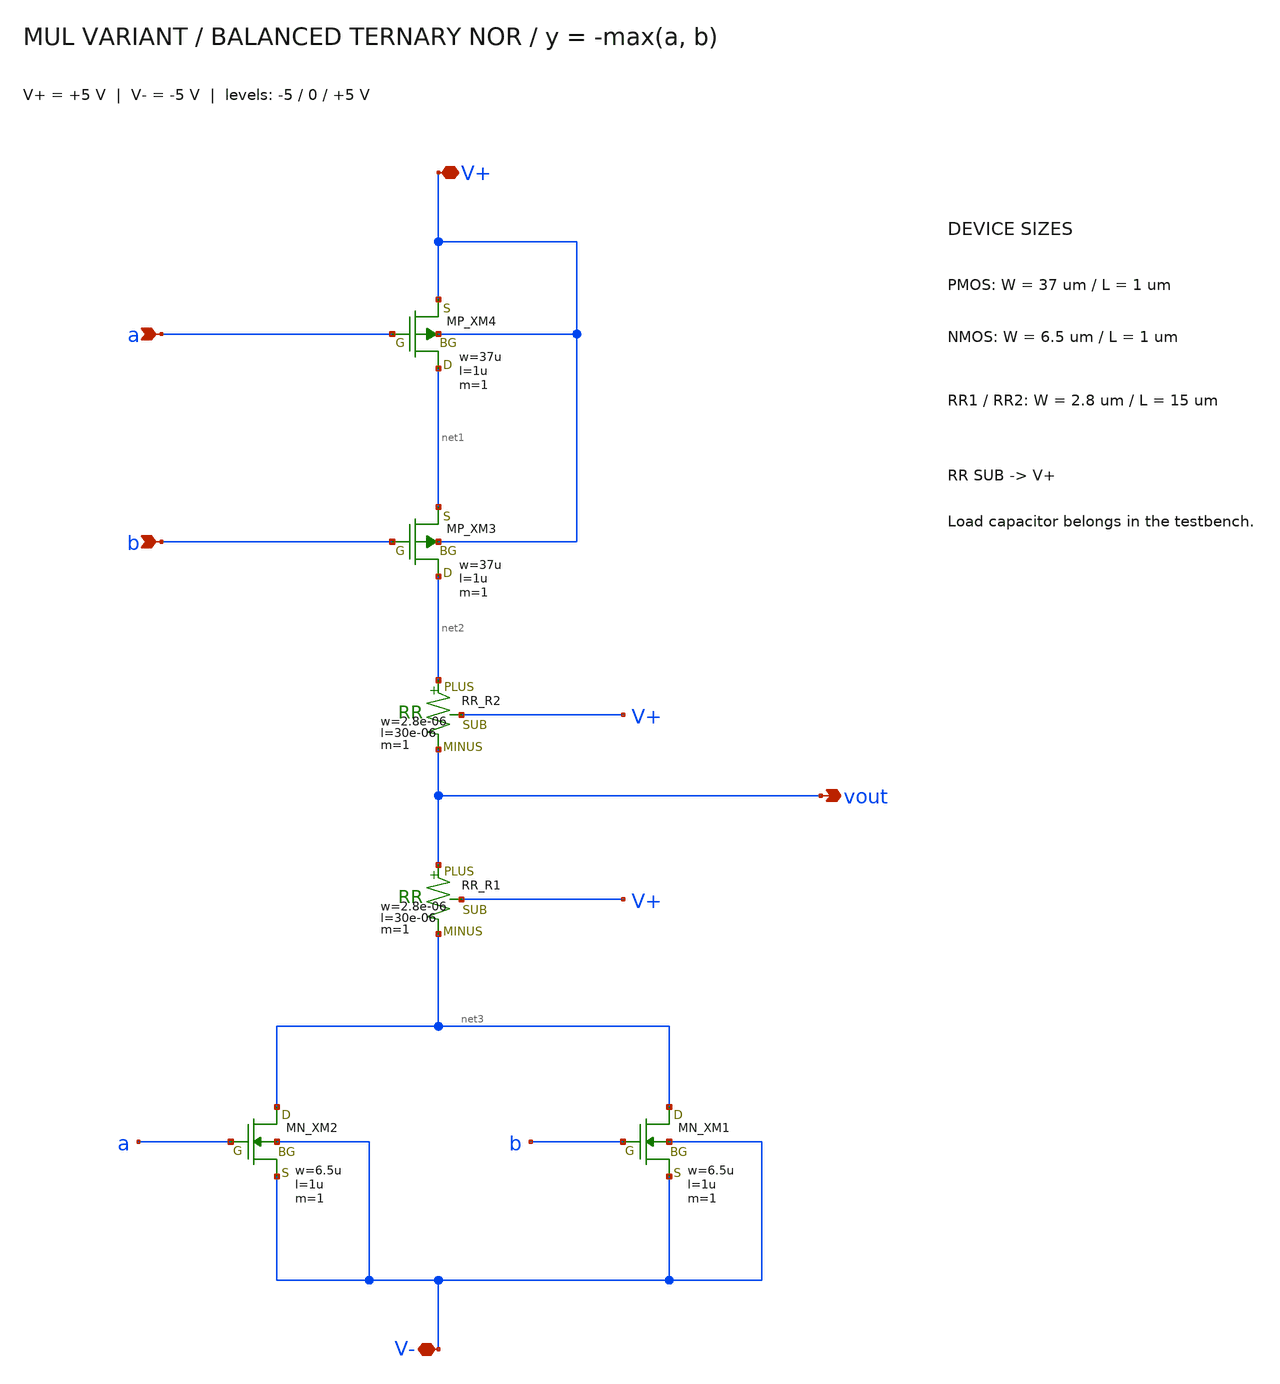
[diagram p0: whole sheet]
** sch_path: member_project/balanced-ternary-logic/PenguinEino/submission/mul_nor.sch
**.subckt mul_nor V+ a b vout V-
*.iopin V+
*.ipin a
*.ipin b
*.opin vout
*.iopin V-
XXM4 net1 a V+ V+ PMOS w=37u l=1u nrd=0 nrs=0 m=1
XXM3 net2 b net1 V+ PMOS w=37u l=1u nrd=0 nrs=0 m=1
XR2 net2 vout V+ F_RR w=2.8e-06 l=30e-06 R=1 tc1=0 tc2=0 m=1
XR1 vout net3 V+ F_RR w=2.8e-06 l=30e-06 R=1 tc1=0 tc2=0 m=1
XXM2 net3 a V- V- NMOS w=6.5u l=1u nrd=0 nrs=0 m=1
XXM1 net3 b V- V- NMOS w=6.5u l=1u nrd=0 nrs=0 m=1
**.ends
.end
